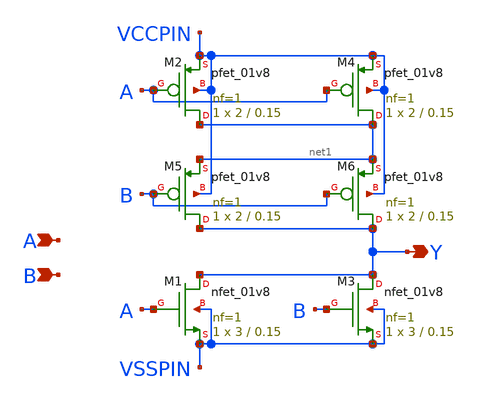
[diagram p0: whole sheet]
** sch_path: lib/xschem/NOR2X1.sch
**.subckt NOR2X1 A Y B
*.ipin A
*.opin Y
*.ipin B
XM1 Y A VSSPIN VSSPIN sky130_fd_pr__nfet_01v8 L=0.15 W=3 nf=1 ad='int((nf+1)/2) * W/nf * 0.29' as='int((nf+2)/2) * W/nf * 0.29'
+ pd='2*int((nf+1)/2) * (W/nf + 0.29)' ps='2*int((nf+2)/2) * (W/nf + 0.29)' nrd='0.29 / W' nrs='0.29 / W'
+ sa=0 sb=0 sd=0 mult=1 m=1
XM2 net1 A VCCPIN VCCPIN sky130_fd_pr__pfet_01v8 L=0.15 W=2 nf=1 ad='int((nf+1)/2) * W/nf * 0.29' as='int((nf+2)/2) * W/nf * 0.29'
+ pd='2*int((nf+1)/2) * (W/nf + 0.29)' ps='2*int((nf+2)/2) * (W/nf + 0.29)' nrd='0.29 / W' nrs='0.29 / W'
+ sa=0 sb=0 sd=0 mult=1 m=1
XM3 Y B VSSPIN VSSPIN sky130_fd_pr__nfet_01v8 L=0.15 W=3 nf=1 ad='int((nf+1)/2) * W/nf * 0.29' as='int((nf+2)/2) * W/nf * 0.29'
+ pd='2*int((nf+1)/2) * (W/nf + 0.29)' ps='2*int((nf+2)/2) * (W/nf + 0.29)' nrd='0.29 / W' nrs='0.29 / W'
+ sa=0 sb=0 sd=0 mult=1 m=1
XM4 net1 A VCCPIN VCCPIN sky130_fd_pr__pfet_01v8 L=0.15 W=2 nf=1 ad='int((nf+1)/2) * W/nf * 0.29' as='int((nf+2)/2) * W/nf * 0.29'
+ pd='2*int((nf+1)/2) * (W/nf + 0.29)' ps='2*int((nf+2)/2) * (W/nf + 0.29)' nrd='0.29 / W' nrs='0.29 / W'
+ sa=0 sb=0 sd=0 mult=1 m=1
XM5 Y B net1 VCCPIN sky130_fd_pr__pfet_01v8 L=0.15 W=2 nf=1 ad='int((nf+1)/2) * W/nf * 0.29' as='int((nf+2)/2) * W/nf * 0.29'
+ pd='2*int((nf+1)/2) * (W/nf + 0.29)' ps='2*int((nf+2)/2) * (W/nf + 0.29)' nrd='0.29 / W' nrs='0.29 / W'
+ sa=0 sb=0 sd=0 mult=1 m=1
XM6 Y B net1 VCCPIN sky130_fd_pr__pfet_01v8 L=0.15 W=2 nf=1 ad='int((nf+1)/2) * W/nf * 0.29' as='int((nf+2)/2) * W/nf * 0.29'
+ pd='2*int((nf+1)/2) * (W/nf + 0.29)' ps='2*int((nf+2)/2) * (W/nf + 0.29)' nrd='0.29 / W' nrs='0.29 / W'
+ sa=0 sb=0 sd=0 mult=1 m=1
**.ends
.end
